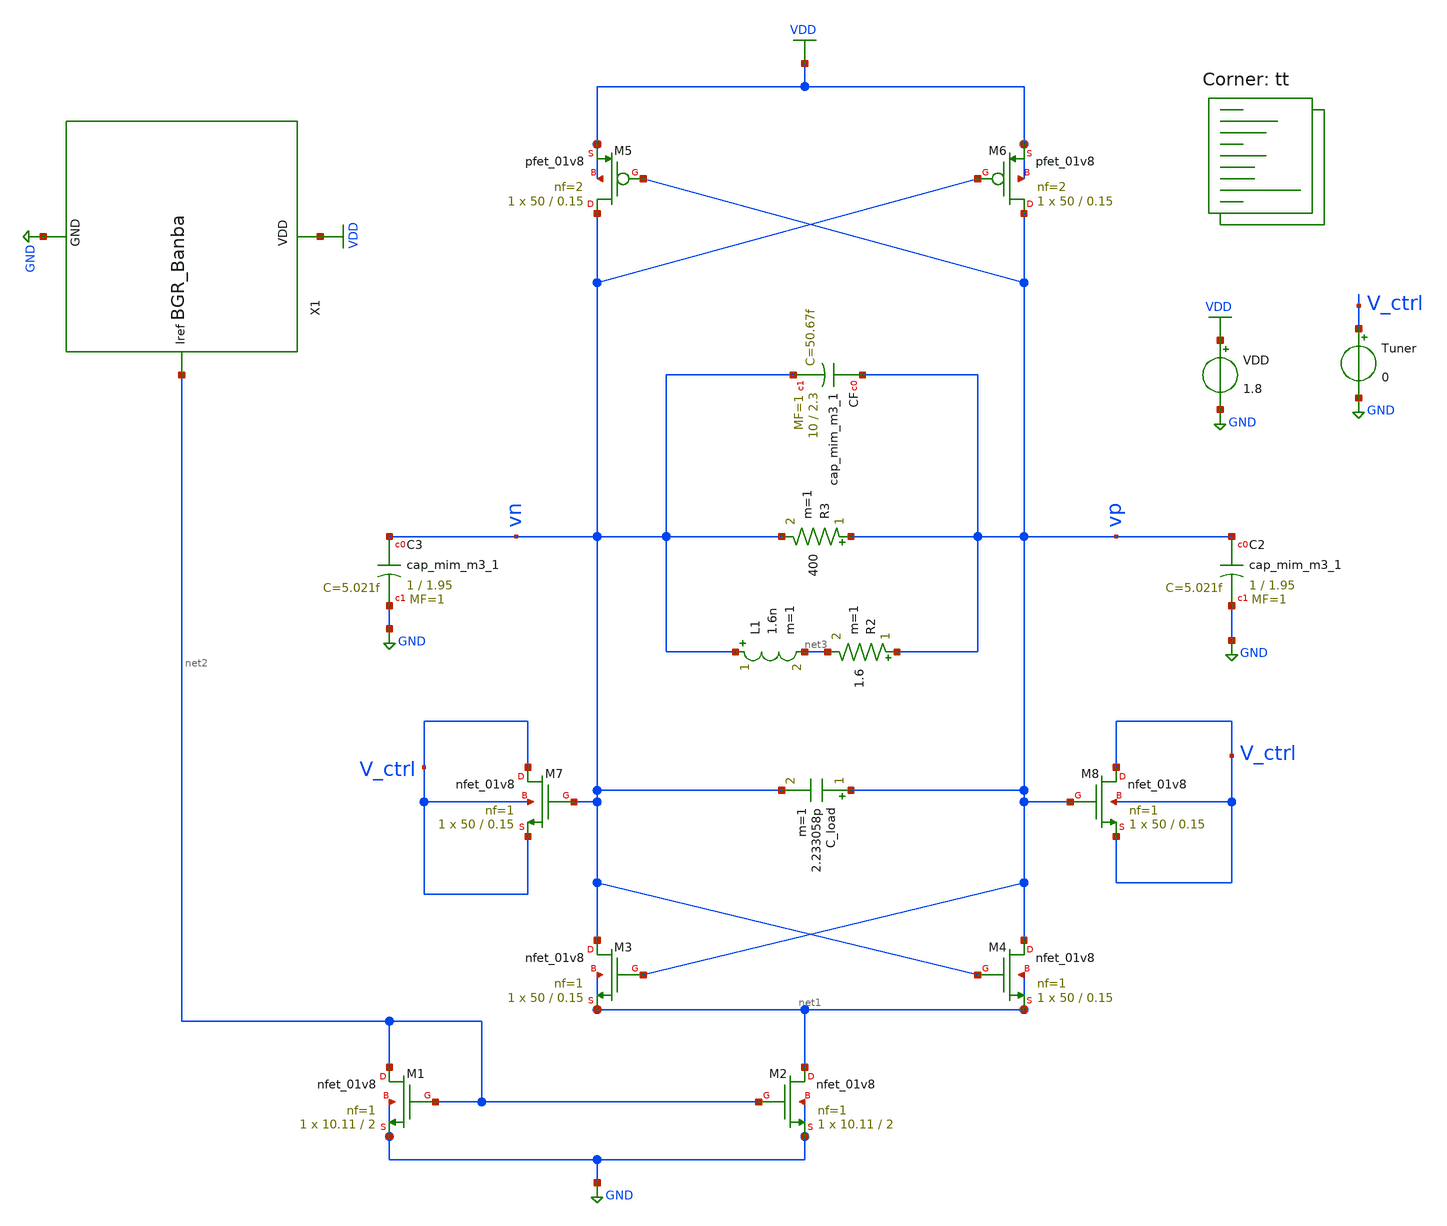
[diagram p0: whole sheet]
** sch_path: pll/lc_vco_lib/Ahmed_Elshahat/CMOS_VCO_with_bias_cct/spice_files/tempo.sch
**.subckt tempo
VDD VDD GND 1.8
XM4 vp vn net1 net1 sky130_fd_pr__nfet_01v8 L=0.15 W=50 nf=1 ad='int((1 + 1)/2) * 50 / 1 * 0.29' as='int((1 + 2)/2) * 50 / 1 * 0.29'
+ pd='2*int((1 + 1)/2) * (50 / 1 + 0.29)' ps='2*int((1 + 2)/2) * (50 / 1 + 0.29)' nrd='0.29 / 50 ' nrs='0.29 / 50 '
+ sa=0 sb=0 sd=0 mult=1 m=1
XM3 vn vp net1 net1 sky130_fd_pr__nfet_01v8 L=0.15 W=50 nf=1 ad='int((1 + 1)/2) * 50 / 1 * 0.29' as='int((1 + 2)/2) * 50 / 1 * 0.29'
+ pd='2*int((1 + 1)/2) * (50 / 1 + 0.29)' ps='2*int((1 + 2)/2) * (50 / 1 + 0.29)' nrd='0.29 / 50 ' nrs='0.29 / 50 '
+ sa=0 sb=0 sd=0 mult=1 m=1
XM1 net2 net2 GND GND sky130_fd_pr__nfet_01v8 L=2 W=10.11 nf=1 ad='int((1 + 1)/2) * 10.11 / 1 * 0.29'
+ as='int((1 + 2)/2) * 10.11 / 1 * 0.29' pd='2*int((1 + 1)/2) * (10.11 / 1 + 0.29)' ps='2*int((1 + 2)/2) * (10.11 / 1 + 0.29)'
+ nrd='0.29 / 10.11 ' nrs='0.29 / 10.11 ' sa=0 sb=0 sd=0 mult=1 m=1
L1 vn net3 1.6n m=1
R2 vp net3 1.6 m=1
XCF vp vn sky130_fd_pr__cap_mim_m3_1 W=10 L=2.3 MF=1 m=1
R3 vp vn 400 m=1
XM5 vn vp VDD VDD sky130_fd_pr__pfet_01v8 L=0.15 W=50 nf=2 ad='int((nf+1)/2) * W/nf * 0.29' as='int((nf+2)/2) * W/nf * 0.29'
+ pd='2*int((nf+1)/2) * (W/nf + 0.29)' ps='2*int((nf+2)/2) * (W/nf + 0.29)' nrd='0.29 / W' nrs='0.29 / W'
+ sa=0 sb=0 sd=0 mult=1 m=1
XM6 vp vn VDD VDD sky130_fd_pr__pfet_01v8 L=0.15 W=50 nf=2 ad='int((nf+1)/2) * W/nf * 0.29' as='int((nf+2)/2) * W/nf * 0.29'
+ pd='2*int((nf+1)/2) * (W/nf + 0.29)' ps='2*int((nf+2)/2) * (W/nf + 0.29)' nrd='0.29 / W' nrs='0.29 / W'
+ sa=0 sb=0 sd=0 mult=1 m=1
XC3 vn GND sky130_fd_pr__cap_mim_m3_1 W=1 L=1.95 MF=1 m=1
XC2 vp GND sky130_fd_pr__cap_mim_m3_1 W=1 L=1.95 MF=1 m=1
XM2 net1 net2 GND GND sky130_fd_pr__nfet_01v8 L=2 W=10.11 nf=1 ad='int((1 + 1)/2) * 10.11 / 1 * 0.29'
+ as='int((1 + 2)/2) * 10.11 / 1 * 0.29' pd='2*int((1 + 1)/2) * (10.11 / 1 + 0.29)' ps='2*int((1 + 2)/2) * (10.11 / 1 + 0.29)'
+ nrd='0.29 / 10.11 ' nrs='0.29 / 10.11 ' sa=0 sb=0 sd=0 mult=1 m=1
C_load vp vn 2.233058p m=1
XM8 V_ctrl vp V_ctrl V_ctrl sky130_fd_pr__nfet_01v8 L=0.15 W=50 nf=1 ad='int((1 + 1)/2) * 50 / 1 * 0.29'
+ as='int((1 + 2)/2) * 50 / 1 * 0.29' pd='2*int((1 + 1)/2) * (50 / 1 + 0.29)' ps='2*int((1 + 2)/2) * (50 / 1 + 0.29)'
+ nrd='0.29 / 50 ' nrs='0.29 / 50 ' sa=0 sb=0 sd=0 mult=1 m=1
XM7 V_ctrl vn V_ctrl V_ctrl sky130_fd_pr__nfet_01v8 L=0.15 W=50 nf=1 ad='int((1 + 1)/2) * 50 / 1 * 0.29'
+ as='int((1 + 2)/2) * 50 / 1 * 0.29' pd='2*int((1 + 1)/2) * (50 / 1 + 0.29)' ps='2*int((1 + 2)/2) * (50 / 1 + 0.29)'
+ nrd='0.29 / 50 ' nrs='0.29 / 50 ' sa=0 sb=0 sd=0 mult=1 m=1
Tuner V_ctrl GND 0
X1 net2 GND VDD BGR_Banba
**** begin user architecture code
.lib $::SKYWATER_MODELS/sky130.lib.spice tt
**** end user architecture code
**.ends
.GLOBAL GND
.GLOBAL VDD
.end
